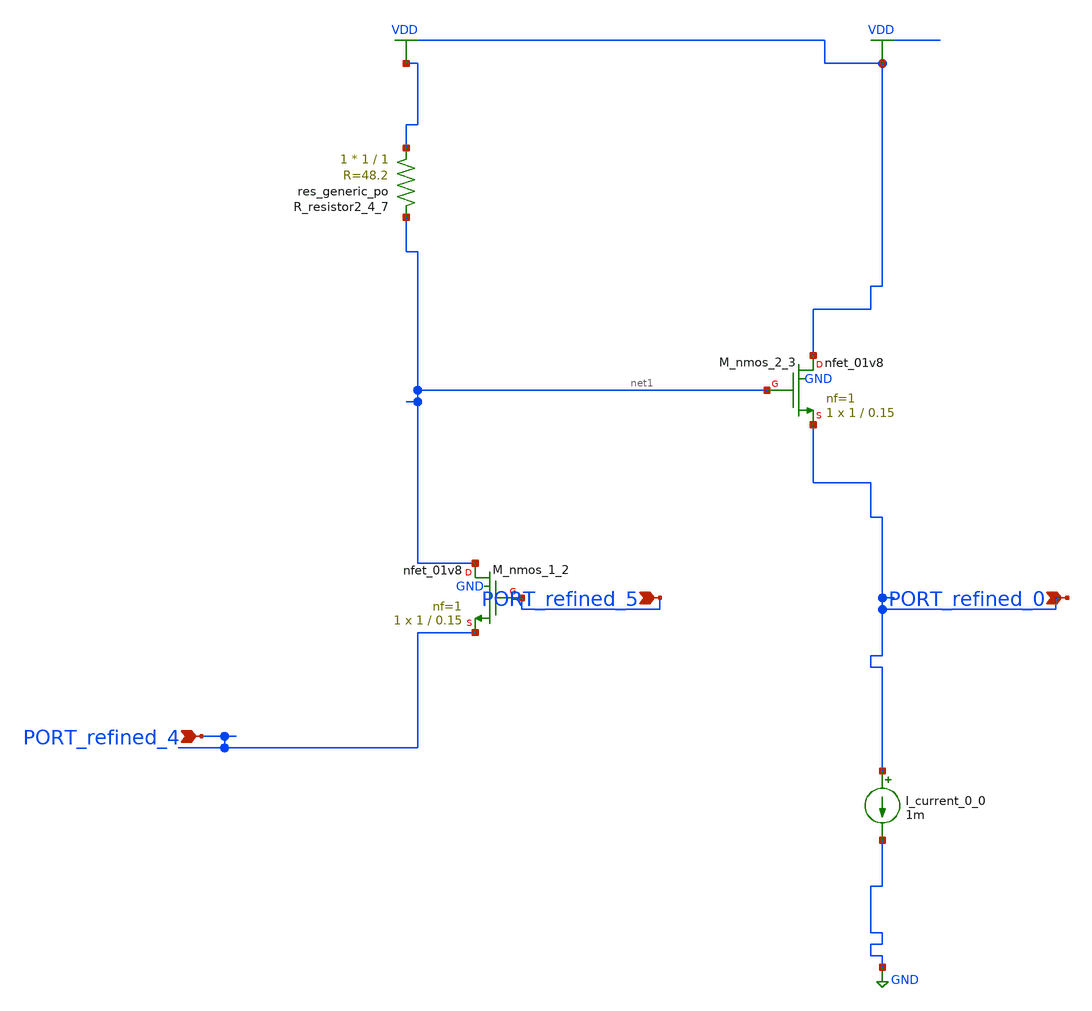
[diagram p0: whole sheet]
** sch_path: schematics/AMSNet/549.sch
**.subckt 549 PORT_refined_5 PORT_refined_0 PORT_refined_4
*.ipin PORT_refined_5
*.ipin PORT_refined_0
*.ipin PORT_refined_4
I_current_0_0 PORT_refined_0 GND 1m
XM_nmos_1_2 net1 PORT_refined_5 PORT_refined_4 GND sky130_fd_pr__nfet_01v8 L=0.15 W=1 nf=1 ad='int((1 + 1)/2) * 1 / 1 * 0.29'
+ as='int((1 + 2)/2) * 1 / 1 * 0.29' pd='2*int((1 + 1)/2) * (1 / 1 + 0.29)' ps='2*int((1 + 2)/2) * (1 / 1 + 0.29)'
+ nrd='0.29 / 1 ' nrs='0.29 / 1 ' sa=0 sb=0 sd=0 mult=1 m=1
XM_nmos_2_3 VDD net1 PORT_refined_0 GND sky130_fd_pr__nfet_01v8 L=0.15 W=1 nf=1 ad='int((1 + 1)/2) * 1 / 1 * 0.29'
+ as='int((1 + 2)/2) * 1 / 1 * 0.29' pd='2*int((1 + 1)/2) * (1 / 1 + 0.29)' ps='2*int((1 + 2)/2) * (1 / 1 + 0.29)'
+ nrd='0.29 / 1 ' nrs='0.29 / 1 ' sa=0 sb=0 sd=0 mult=1 m=1
XR_resistor2_4_7 VDD net1 sky130_fd_pr__res_generic_po W=1 L=1 m=1
**.ends
.GLOBAL GND
.GLOBAL VDD
.end
